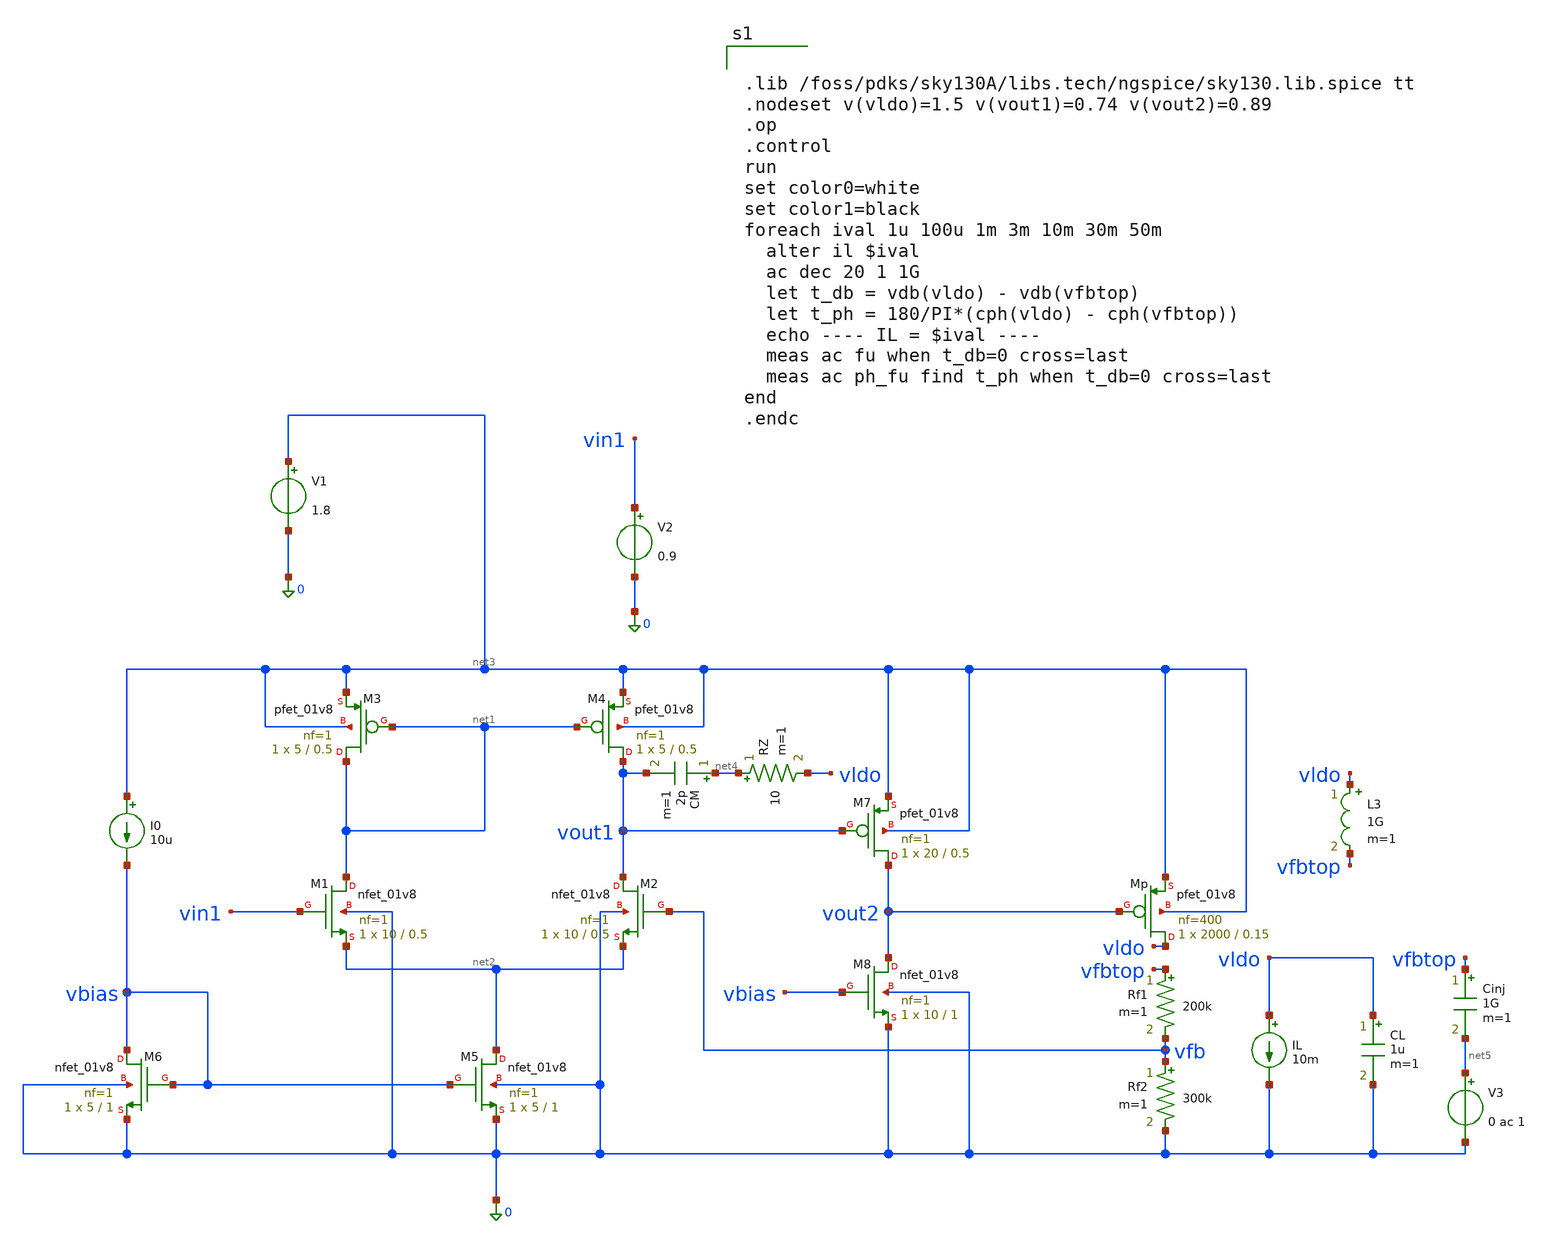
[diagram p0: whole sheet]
** sch_path: src/schematics/ldo_top.sch
**.subckt ldo_top
XM1 net1 vin1 net2 0 sky130_fd_pr__nfet_01v8 L=0.5 W=10 nf=1 ad='int((1 + 1)/2) * 10 / 1 * 0.29' as='int((1 + 2)/2) * 10 / 1 * 0.29'
+ pd='2*int((1 + 1)/2) * (10 / 1 + 0.29)' ps='2*int((1 + 2)/2) * (10 / 1 + 0.29)' nrd='0.29 / 10 ' nrs='0.29 / 10 '
+ sa=0 sb=0 sd=0 mult=1 m=1
XM2 vout1 vfb net2 0 sky130_fd_pr__nfet_01v8 L=0.5 W=10 nf=1 ad='int((1 + 1)/2) * 10 / 1 * 0.29' as='int((1 + 2)/2) * 10 / 1 * 0.29'
+ pd='2*int((1 + 1)/2) * (10 / 1 + 0.29)' ps='2*int((1 + 2)/2) * (10 / 1 + 0.29)' nrd='0.29 / 10 ' nrs='0.29 / 10 '
+ sa=0 sb=0 sd=0 mult=1 m=1
XM3 net1 net1 net3 net3 sky130_fd_pr__pfet_01v8 L=0.5 W=5 nf=1 ad='int((1 + 1)/2) * 5 / 1 * 0.29' as='int((1 + 2)/2) * 5 / 1 * 0.29'
+ pd='2*int((1 + 1)/2) * (5 / 1 + 0.29)' ps='2*int((1 + 2)/2) * (5 / 1 + 0.29)' nrd='0.29 / 5 ' nrs='0.29 / 5 '
+ sa=0 sb=0 sd=0 mult=1 m=1
XM4 vout1 net1 net3 net3 sky130_fd_pr__pfet_01v8 L=0.5 W=5 nf=1 ad='int((1 + 1)/2) * 5 / 1 * 0.29' as='int((1 + 2)/2) * 5 / 1 * 0.29'
+ pd='2*int((1 + 1)/2) * (5 / 1 + 0.29)' ps='2*int((1 + 2)/2) * (5 / 1 + 0.29)' nrd='0.29 / 5 ' nrs='0.29 / 5 '
+ sa=0 sb=0 sd=0 mult=1 m=1
XM5 net2 vbias 0 0 sky130_fd_pr__nfet_01v8 L=1 W=5 nf=1 ad='int((1 + 1)/2) * 5 / 1 * 0.29' as='int((1 + 2)/2) * 5 / 1 * 0.29'
+ pd='2*int((1 + 1)/2) * (5 / 1 + 0.29)' ps='2*int((1 + 2)/2) * (5 / 1 + 0.29)' nrd='0.29 / 5 ' nrs='0.29 / 5 '
+ sa=0 sb=0 sd=0 mult=1 m=1
XM6 vbias vbias 0 0 sky130_fd_pr__nfet_01v8 L=1 W=5 nf=1 ad='int((1 + 1)/2) * 5 / 1 * 0.29' as='int((1 + 2)/2) * 5 / 1 * 0.29'
+ pd='2*int((1 + 1)/2) * (5 / 1 + 0.29)' ps='2*int((1 + 2)/2) * (5 / 1 + 0.29)' nrd='0.29 / 5 ' nrs='0.29 / 5 '
+ sa=0 sb=0 sd=0 mult=1 m=1
I0 net3 vbias 10u
V1 net3 0 1.8
V2 vin1 0 0.9
XM7 vout2 vout1 net3 net3 sky130_fd_pr__pfet_01v8 L=0.5 W=20 nf=1 ad='int((1 + 1)/2) * 20 / 1 * 0.29'
+ as='int((1 + 2)/2) * 20 / 1 * 0.29' pd='2*int((1 + 1)/2) * (20 / 1 + 0.29)' ps='2*int((1 + 2)/2) * (20 / 1 + 0.29)'
+ nrd='0.29 / 20 ' nrs='0.29 / 20 ' sa=0 sb=0 sd=0 mult=1 m=1
XM8 vout2 vbias 0 0 sky130_fd_pr__nfet_01v8 L=1 W=10 nf=1 ad='int((1 + 1)/2) * 10 / 1 * 0.29' as='int((1 + 2)/2) * 10 / 1 * 0.29'
+ pd='2*int((1 + 1)/2) * (10 / 1 + 0.29)' ps='2*int((1 + 2)/2) * (10 / 1 + 0.29)' nrd='0.29 / 10 ' nrs='0.29 / 10 '
+ sa=0 sb=0 sd=0 mult=1 m=1
CM net4 vout1 2p m=1
RZ net4 vldo 10 m=1
Rf1 vfbtop vfb 200k m=1
Rf2 vfb 0 300k m=1
CL vldo 0 1u m=1
IL vldo 0 10m
XMp vldo vout2 net3 net3 sky130_fd_pr__pfet_01v8 L=0.15 W=2000 nf=400 ad='int((400 + 1)/2) * 2000 / 400 * 0.29'
+ as='int((400 + 2)/2) * 2000 / 400 * 0.29' pd='2*int((400 + 1)/2) * (2000 / 400 + 0.29)' ps='2*int((400 + 2)/2) * (2000 / 400 + 0.29)'
+ nrd='0.29 / 2000 ' nrs='0.29 / 2000 ' sa=0 sb=0 sd=0 mult=1 m=1
L3 vldo vfbtop 1G m=1
Cinj vfbtop net5 1G m=1
V3 net5 0 0 ac 1
**** begin user architecture code


.lib /foss/pdks/sky130A/libs.tech/ngspice/sky130.lib.spice tt
.nodeset v(vldo)=1.5 v(vout1)=0.74 v(vout2)=0.89
.op
.control
run
set color0=white
set color1=black
foreach ival 1u 100u 1m 3m 10m 30m 50m
  alter il $ival
  ac dec 20 1 1G
  let t_db = vdb(vldo) - vdb(vfbtop)
  let t_ph = 180/PI*(cph(vldo) - cph(vfbtop))
  echo ---- IL = $ival ----
  meas ac fu when t_db=0 cross=last
  meas ac ph_fu find t_ph when t_db=0 cross=last
end
.endc


**** end user architecture code
**.ends
.end
